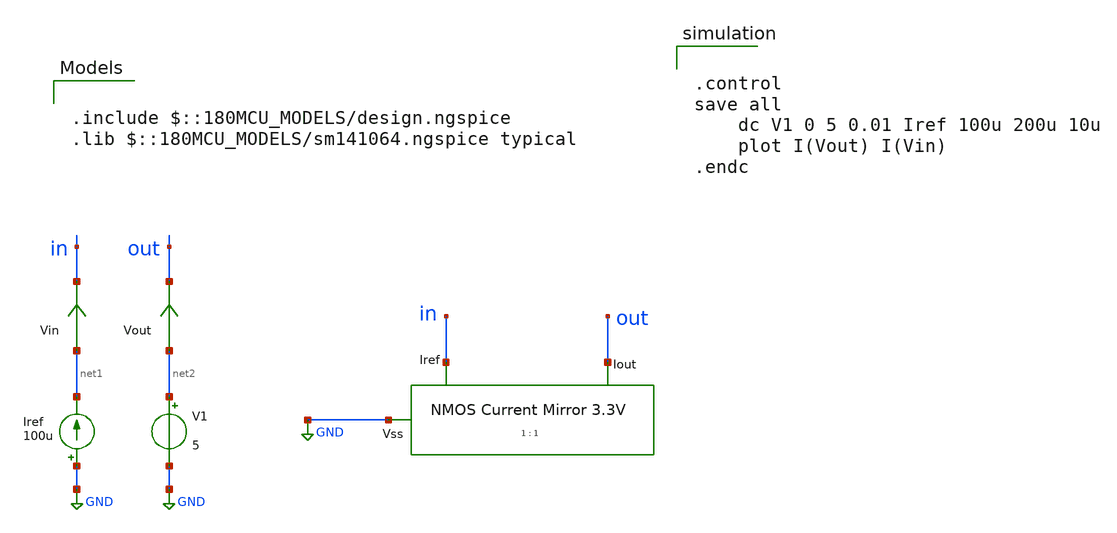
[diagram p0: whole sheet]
** sch_path: designs/libs/tb_analog/tb_nmos_current_mirror/tb_nmos_current_mirror.sch
**.subckt tb_nmos_current_mirror
Iref GND net1 100u
V1 net2 GND 5
Vin net1 in 0
.save i(vin)
Vout net2 out 0
.save i(vout)
x1 in out GND nmos_current_mirror
**** begin user architecture code


.control
save all
	dc V1 0 5 0.01 Iref 100u 200u 10u
	plot I(Vout) I(Vin)
.endc



.include $::180MCU_MODELS/design.ngspice
.lib $::180MCU_MODELS/sm141064.ngspice typical

**** end user architecture code
**.ends
.GLOBAL GND
.end
